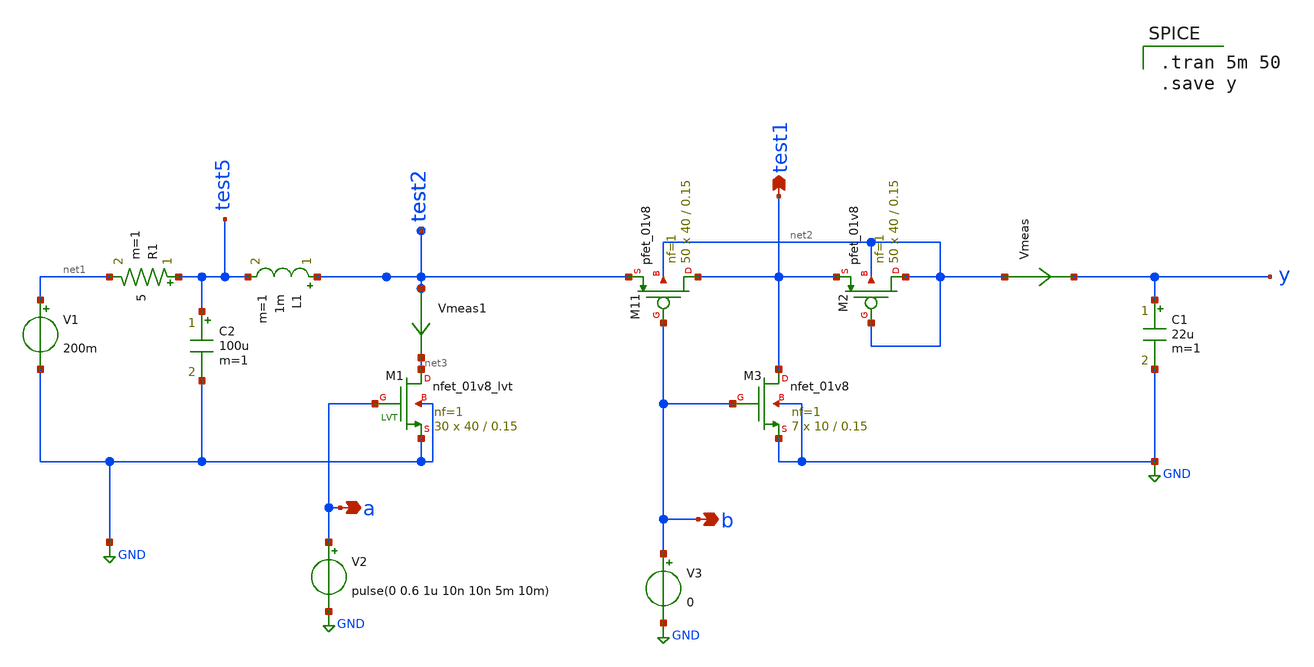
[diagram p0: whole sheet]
** sch_path: component/Core Functionality of boost Converter/vs test4.sch
**.subckt vs test4 a test1 b
*.opin a
*.opin test1
*.opin b
V1 net1 GND 200m
C1 y GND 22u m=1
L1 test2 test5 1m m=1
XM11 test1 b test2 net2 sky130_fd_pr__pfet_01v8 L=0.15 W=40 nf=1 ad='int((nf+1)/2) * W/nf * 0.29' as='int((nf+2)/2) * W/nf * 0.29'
+ pd='2*int((nf+1)/2) * (W/nf + 0.29)' ps='2*int((nf+2)/2) * (W/nf + 0.29)' nrd='0.29 / W' nrs='0.29 / W'
+ sa=0 sb=0 sd=0 mult=50 m=50
V2 a GND pulse(0 0.6 1u 10n 10n 5m 10m)
Vmeas net2 y 0
.save i(vmeas)
Vmeas1 test2 net3 0
.save i(vmeas1)
XM2 net2 net2 test1 net2 sky130_fd_pr__pfet_01v8 L=0.15 W=40 nf=1 ad='int((nf+1)/2) * W/nf * 0.29' as='int((nf+2)/2) * W/nf * 0.29'
+ pd='2*int((nf+1)/2) * (W/nf + 0.29)' ps='2*int((nf+2)/2) * (W/nf + 0.29)' nrd='0.29 / W' nrs='0.29 / W'
+ sa=0 sb=0 sd=0 mult=50 m=50
XM3 test1 b GND GND sky130_fd_pr__nfet_01v8 L=0.15 W=10 nf=1 ad='int((nf+1)/2) * W/nf * 0.29' as='int((nf+2)/2) * W/nf * 0.29'
+ pd='2*int((nf+1)/2) * (W/nf + 0.29)' ps='2*int((nf+2)/2) * (W/nf + 0.29)' nrd='0.29 / W' nrs='0.29 / W'
+ sa=0 sb=0 sd=0 mult=7 m=7
V3 b GND 0
XM1 net3 a GND GND sky130_fd_pr__nfet_01v8_lvt L=0.15 W=40 nf=1 ad='int((nf+1)/2) * W/nf * 0.29' as='int((nf+2)/2) * W/nf * 0.29'
+ pd='2*int((nf+1)/2) * (W/nf + 0.29)' ps='2*int((nf+2)/2) * (W/nf + 0.29)' nrd='0.29 / W' nrs='0.29 / W'
+ sa=0 sb=0 sd=0 mult=30 m=30
R1 test5 net1 5 m=1
C2 test5 GND 100u m=1
**** begin user architecture code

** opencircuitdesign pdks install
.lib $::SKYWATER_MODELS/sky130.lib.spice tt



.tran 5m 50
.save y

**** end user architecture code
**.ends
.GLOBAL GND
.end
